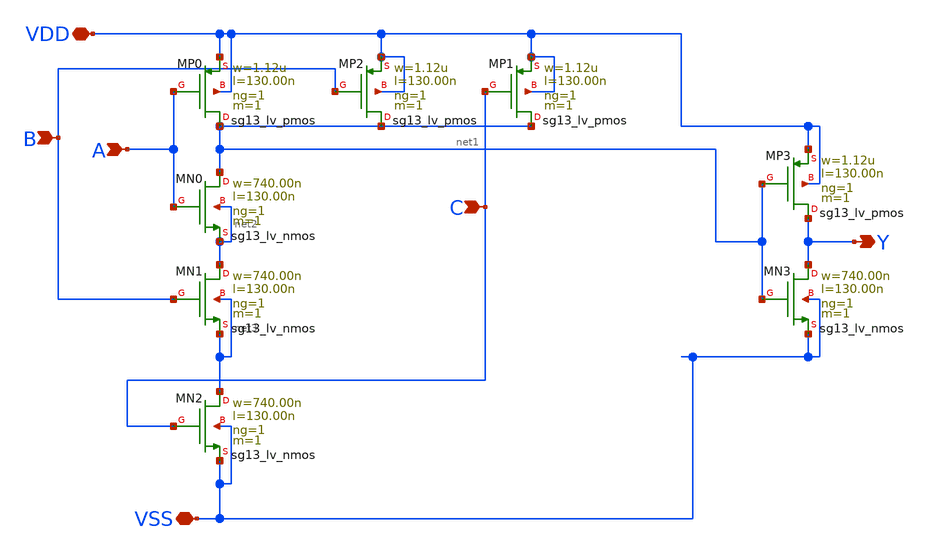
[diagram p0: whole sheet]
** sch_path: xschem/AND.sch
**.subckt AND A VDD B VSS C Y
*.ipin A
*.iopin VDD
*.ipin B
*.iopin VSS
*.ipin C
*.opin Y
XMN0 net1 A net2 net2 sg13_lv_nmos w=740.00n l=130.00n ng=1 m=1 mm_ok=1
XMP0 net1 A VDD VDD sg13_lv_pmos w=1.12u l=130.00n ng=1 m=1 mm_ok=1
XMP1 net1 C VDD VDD sg13_lv_pmos w=1.12u l=130.00n ng=1 m=1 mm_ok=1
XMN1 net2 B net3 net3 sg13_lv_nmos w=740.00n l=130.00n ng=1 m=1 mm_ok=1
XMP2 net1 B VDD VDD sg13_lv_pmos w=1.12u l=130.00n ng=1 m=1 mm_ok=1
XMN2 net3 C VSS VSS sg13_lv_nmos w=740.00n l=130.00n ng=1 m=1 mm_ok=1
XMN3 Y net1 VSS VSS sg13_lv_nmos w=740.00n l=130.00n ng=1 m=1 mm_ok=1
XMP3 Y net1 VDD VDD sg13_lv_pmos w=1.12u l=130.00n ng=1 m=1 mm_ok=1
**.ends
.end
